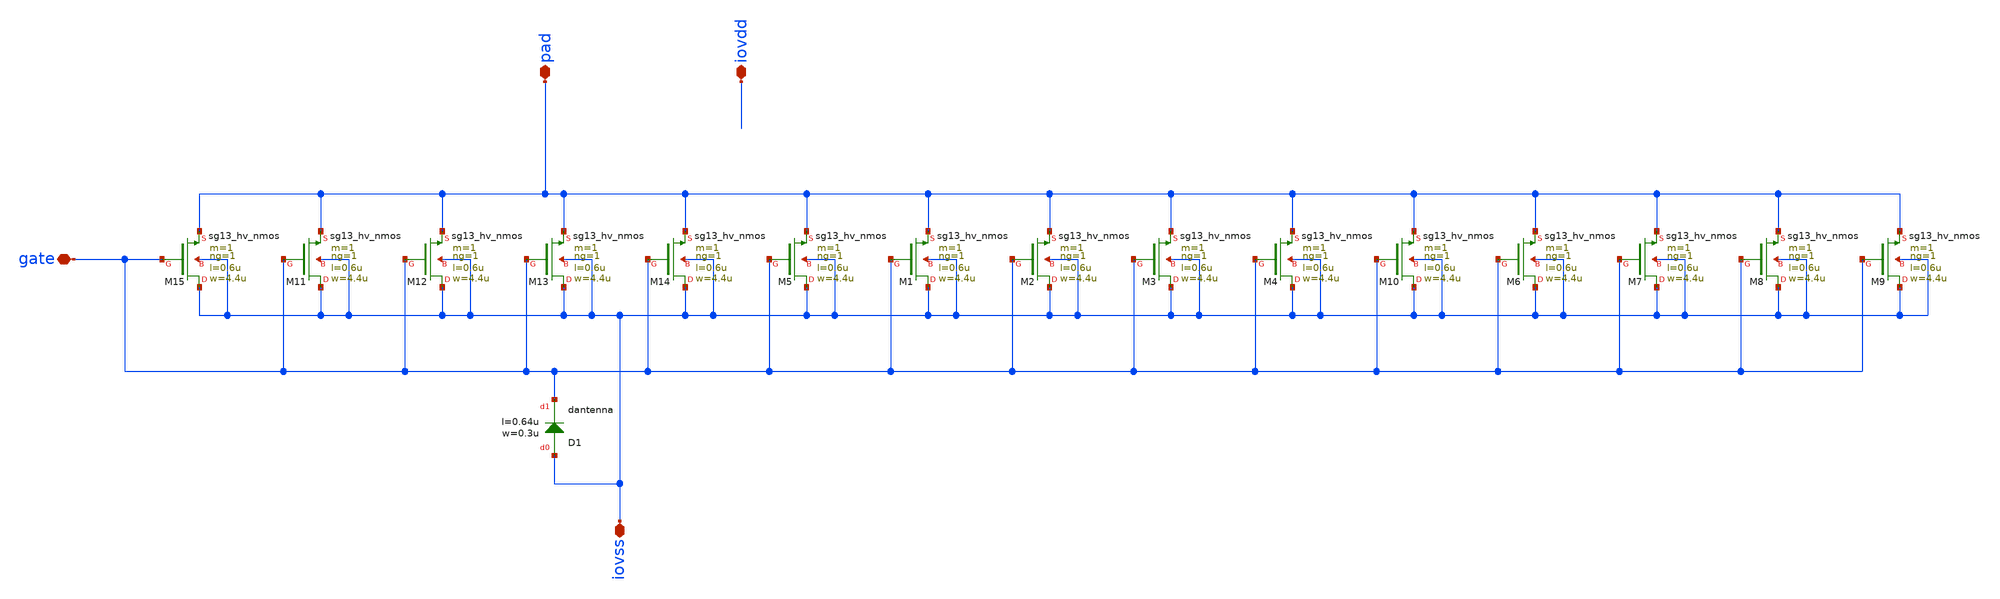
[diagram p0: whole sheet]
** sch_path: ihp-sg13g2/libs.ref/sg13g2_io/xschem/sg13g2_Clamp_N15N15D.sch
**.subckt sg13g2_Clamp_N15N15D iovss gate pad iovdd
*.iopin iovss
*.iopin gate
*.iopin pad
*.iopin iovdd
XM1 iovss gate pad iovss sg13_hv_nmos w=4.4u l=0.6u ng=1 m=1 mm_ok=1
XM2 iovss gate pad iovss sg13_hv_nmos w=4.4u l=0.6u ng=1 m=1 mm_ok=1
XM3 iovss gate pad iovss sg13_hv_nmos w=4.4u l=0.6u ng=1 m=1 mm_ok=1
XM4 iovss gate pad iovss sg13_hv_nmos w=4.4u l=0.6u ng=1 m=1 mm_ok=1
XM5 iovss gate pad iovss sg13_hv_nmos w=4.4u l=0.6u ng=1 m=1 mm_ok=1
XM6 iovss gate pad iovss sg13_hv_nmos w=4.4u l=0.6u ng=1 m=1 mm_ok=1
XM7 iovss gate pad iovss sg13_hv_nmos w=4.4u l=0.6u ng=1 m=1 mm_ok=1
XM8 iovss gate pad iovss sg13_hv_nmos w=4.4u l=0.6u ng=1 m=1 mm_ok=1
XM9 iovss gate pad iovss sg13_hv_nmos w=4.4u l=0.6u ng=1 m=1 mm_ok=1
XM10 iovss gate pad iovss sg13_hv_nmos w=4.4u l=0.6u ng=1 m=1 mm_ok=1
XM11 iovss gate pad iovss sg13_hv_nmos w=4.4u l=0.6u ng=1 m=1 mm_ok=1
XM12 iovss gate pad iovss sg13_hv_nmos w=4.4u l=0.6u ng=1 m=1 mm_ok=1
XM13 iovss gate pad iovss sg13_hv_nmos w=4.4u l=0.6u ng=1 m=1 mm_ok=1
XM14 iovss gate pad iovss sg13_hv_nmos w=4.4u l=0.6u ng=1 m=1 mm_ok=1
XM15 iovss gate pad iovss sg13_hv_nmos w=4.4u l=0.6u ng=1 m=1 mm_ok=1
XD1 iovss gate dantenna l=0.64u w=0.3u
**.ends
.end
